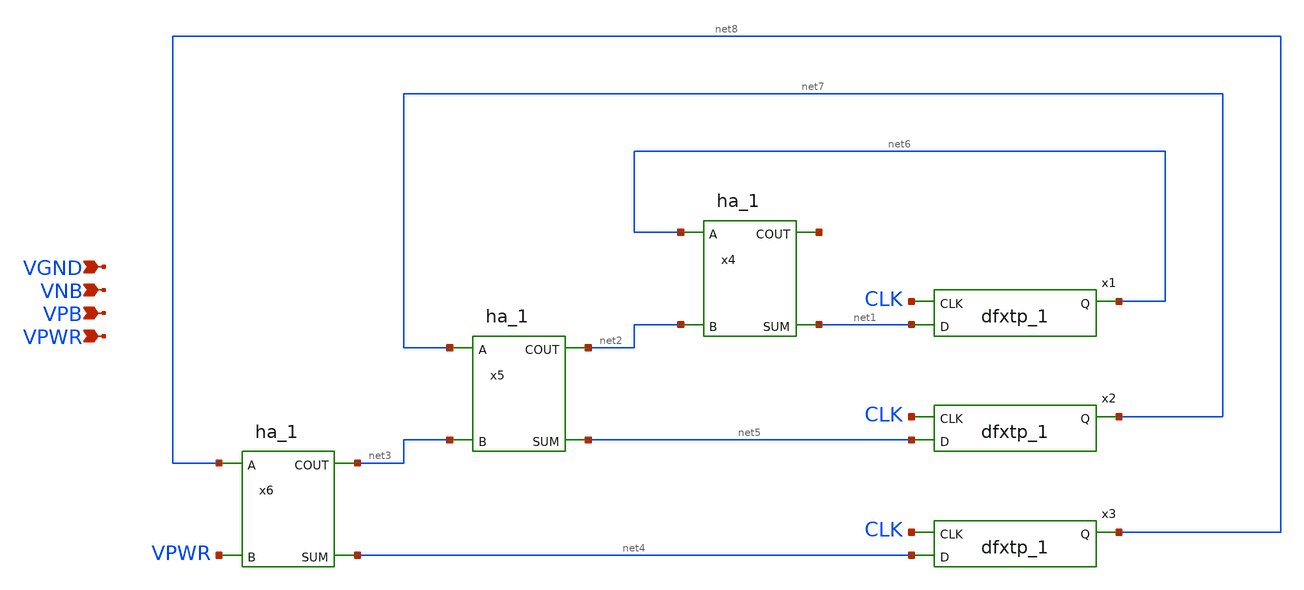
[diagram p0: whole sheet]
** sch_path: project/examples/3bit_counter/3bit_counter.sch
**.subckt 3bit_counter VGND VNB VPB VPWR
*.ipin VGND
*.ipin VNB
*.ipin VPB
*.ipin VPWR
x1 CLK net1 VGND VNB VPB VPWR net6 sky130_fd_sc_hd__dfxtp_1
x2 CLK net5 VGND VNB VPB VPWR net7 sky130_fd_sc_hd__dfxtp_1
x4 net6 net2 VGND VNB VPB VPWR net9 net1 sky130_fd_sc_hd__ha_1
x5 net7 net3 VGND VNB VPB VPWR net2 net5 sky130_fd_sc_hd__ha_1
x3 CLK net4 VGND VNB VPB VPWR net8 sky130_fd_sc_hd__dfxtp_1
x6 net8 VPWR VGND VNB VPB VPWR net3 net4 sky130_fd_sc_hd__ha_1
**.ends
.end
